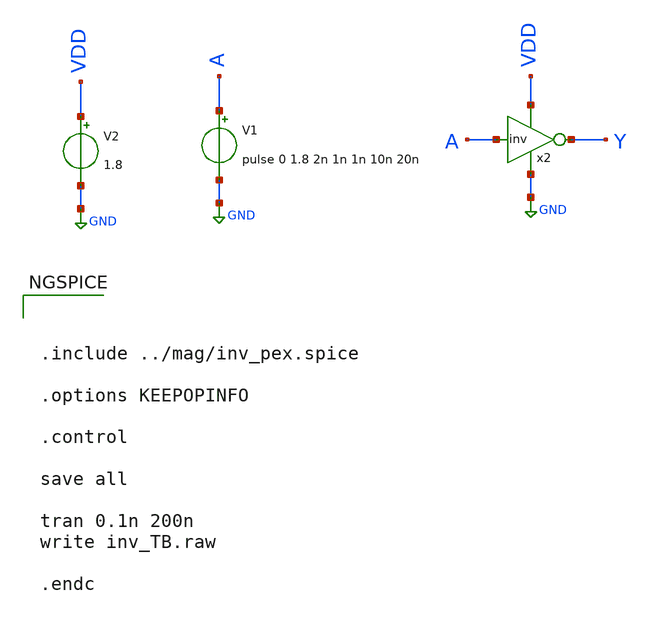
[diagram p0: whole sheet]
** sch_path: examples/xschem/inv_TB.sch
**.subckt inv_TB
V2 VDD GND 1.8
V1 A GND pulse 0 1.8 2n 1n 1n 10n 20n
x2 A VDD Y GND inv
**** begin user architecture code



.include ../mag/inv_pex.spice

.options KEEPOPINFO

.control

save all

tran 0.1n 200n
write inv_TB.raw

.endc



** opencircuitdesign pdks install
.lib $::SKYWATER_MODELS/sky130.lib.spice tt


**** end user architecture code
**.ends
.GLOBAL GND
.end
